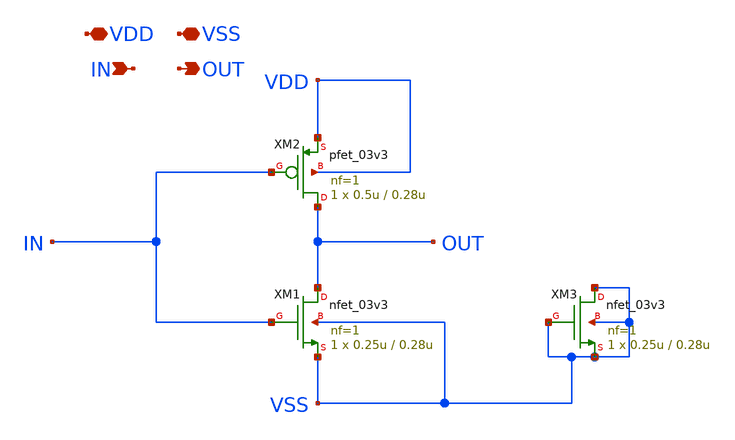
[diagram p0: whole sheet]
** sch_path: AWG_OUTPUT_AND_MUX_PAKISTAN_05/xschem/INVERTER.sch
**.subckt INVERTER VDD VSS IN OUT
*.iopin VDD
*.iopin VSS
*.ipin IN
*.opin OUT
XM1 OUT IN VSS VSS nfet_03v3 L=0.28u W=0.25u nf=1 ad='int((nf+1)/2) * W/nf * 0.18u' as='int((nf+2)/2) * W/nf * 0.18u'
+ pd='2*int((nf+1)/2) * (W/nf + 0.18u)' ps='2*int((nf+2)/2) * (W/nf + 0.18u)' nrd='0.18u / W' nrs='0.18u / W'
+ sa=0 sb=0 sd=0 m=1
XM2 OUT IN VDD VDD pfet_03v3 L=0.28u W=0.5u nf=1 ad='int((nf+1)/2) * W/nf * 0.18u' as='int((nf+2)/2) * W/nf * 0.18u'
+ pd='2*int((nf+1)/2) * (W/nf + 0.18u)' ps='2*int((nf+2)/2) * (W/nf + 0.18u)' nrd='0.18u / W' nrs='0.18u / W'
+ sa=0 sb=0 sd=0 m=1
XM3 VSS VSS VSS VSS nfet_03v3 L=0.28u W=0.25u nf=1 ad='int((nf+1)/2) * W/nf * 0.18u' as='int((nf+2)/2) * W/nf * 0.18u'
+ pd='2*int((nf+1)/2) * (W/nf + 0.18u)' ps='2*int((nf+2)/2) * (W/nf + 0.18u)' nrd='0.18u / W' nrs='0.18u / W'
+ sa=0 sb=0 sd=0 m=1
**.ends
.end
